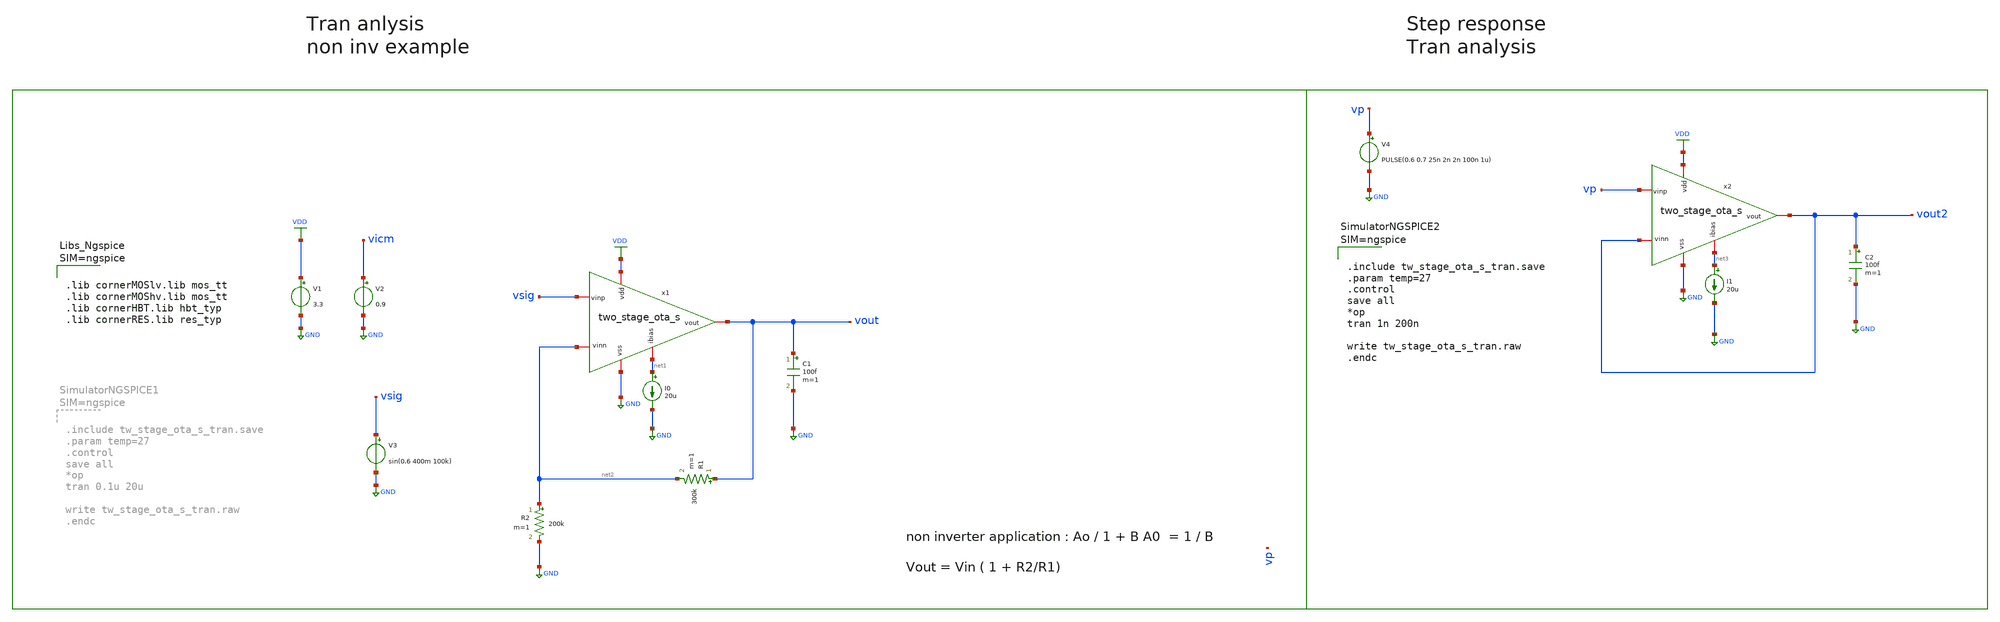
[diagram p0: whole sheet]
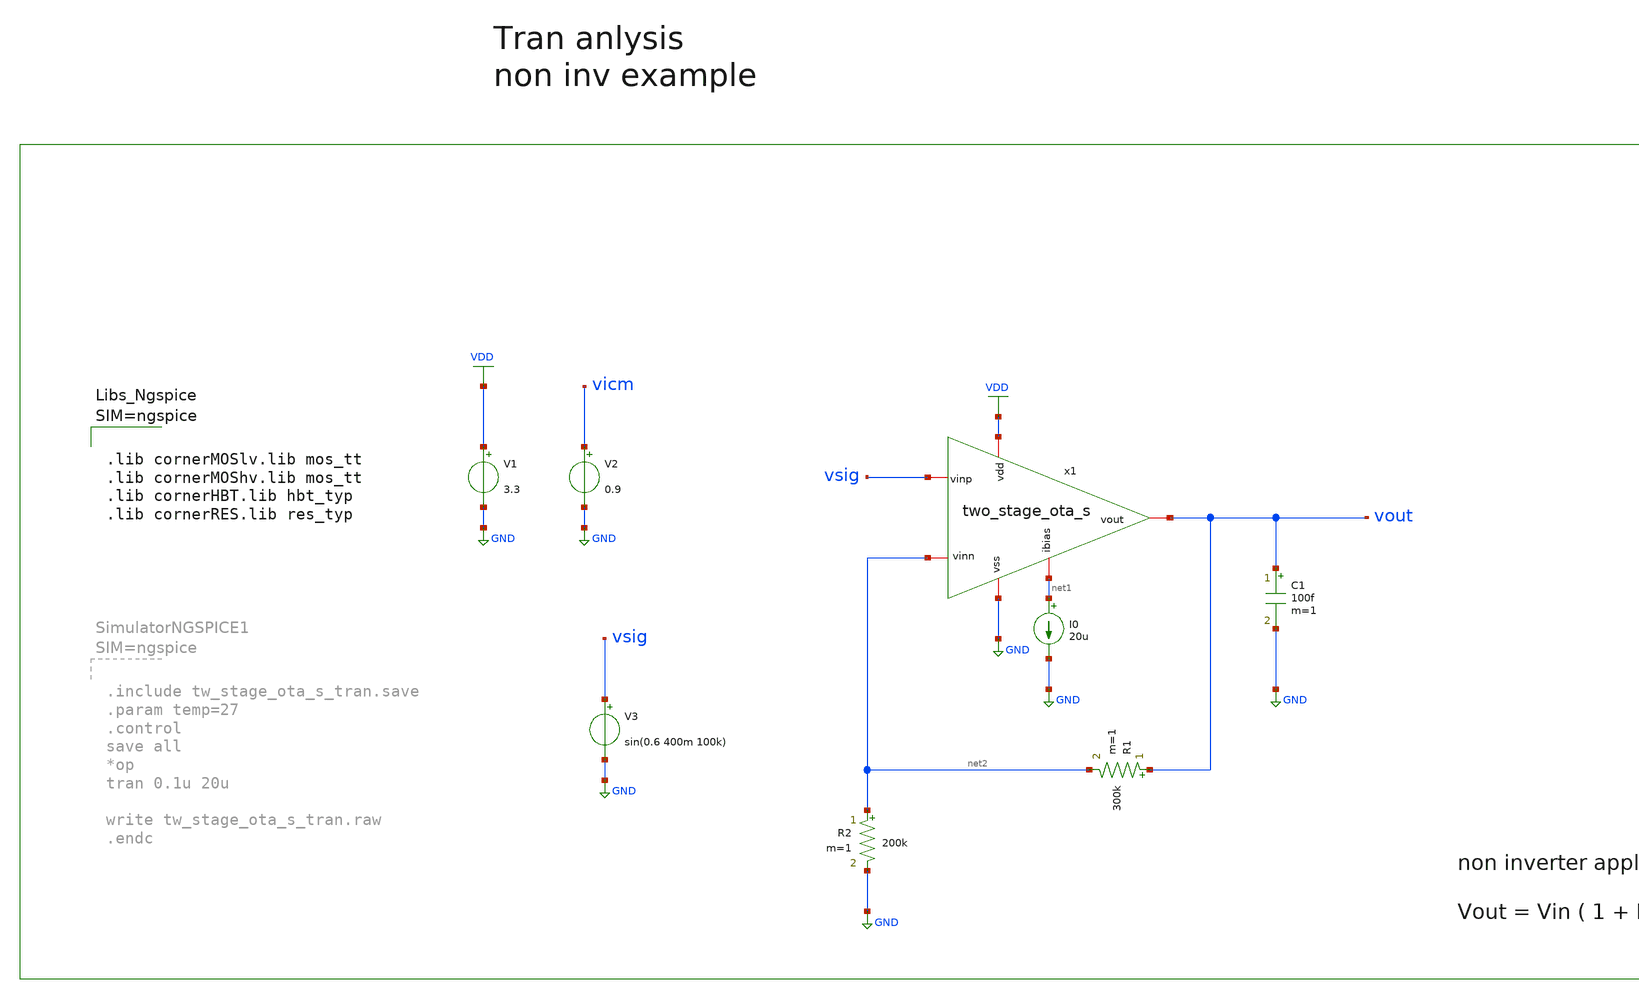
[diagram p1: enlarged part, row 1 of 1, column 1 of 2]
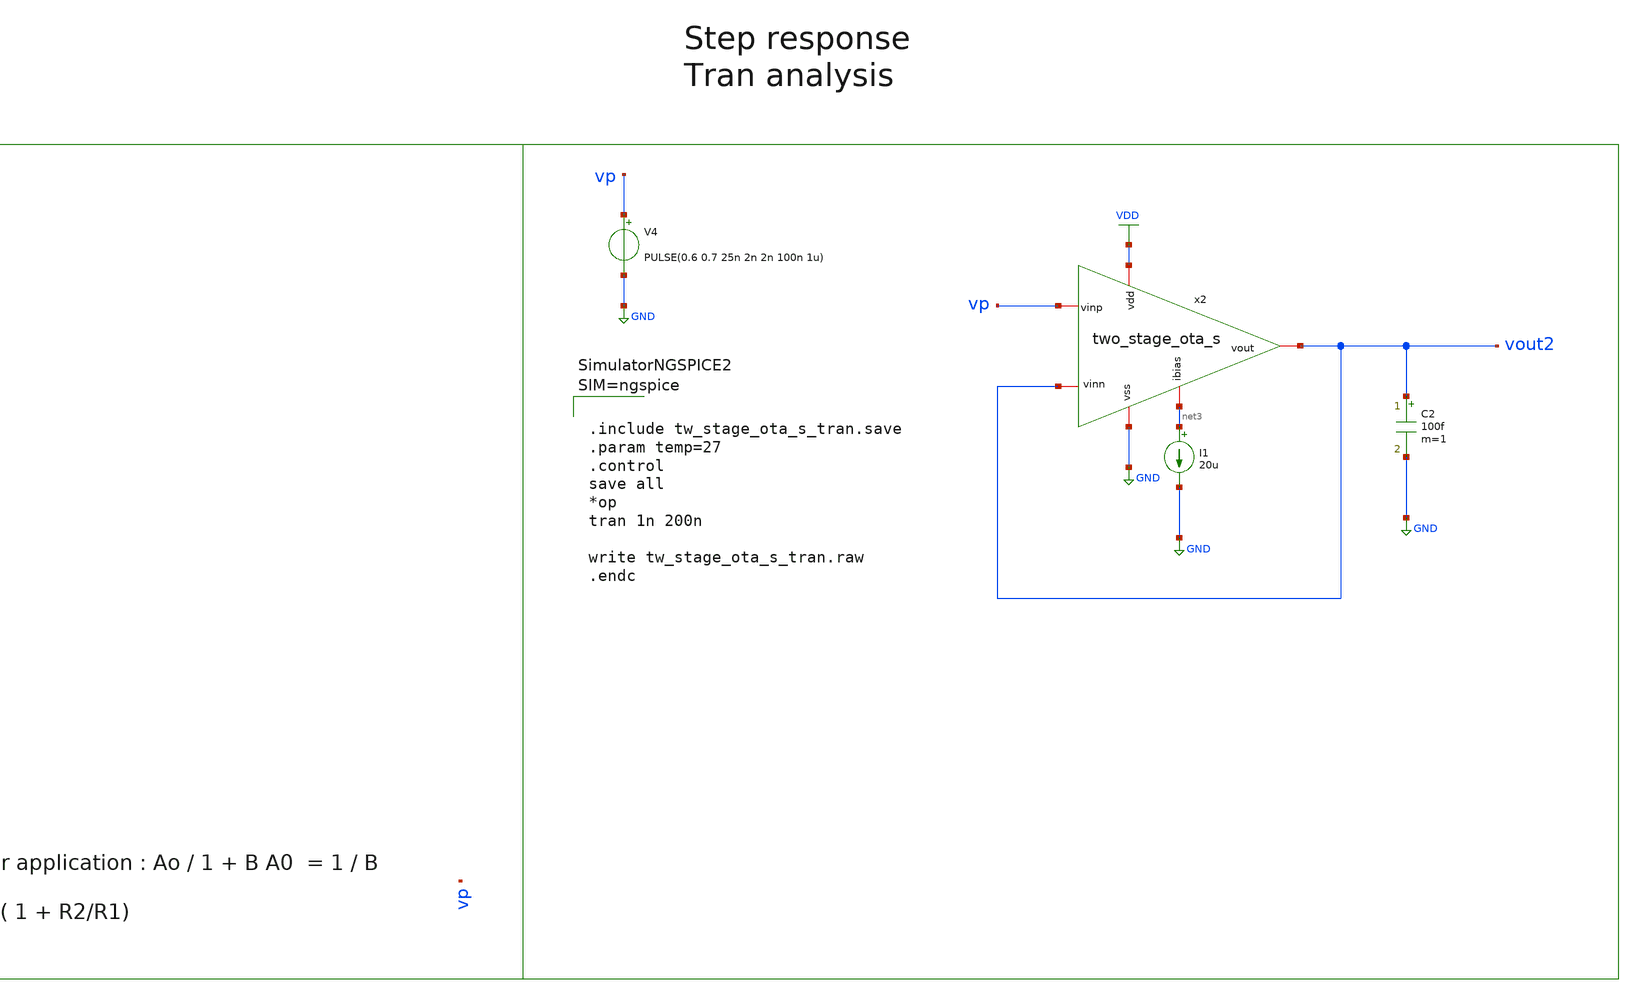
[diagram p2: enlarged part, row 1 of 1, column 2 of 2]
** sch_path: dependencies/pmu_ip/dependencies/OTA/OTA-main/testbenches/tw_stage_ota_s_tran.sch
* (c) 2025-2026 Ider Abdelaziz
**.subckt tw_stage_ota_s_tran
V1 VDD GND 3.3
V2 vicm GND 0.9
V3 vsig GND sin(0.6 400m 100k)
I0 net1 GND 20u
C1 vout GND 100f m=1
R1 vout net2 300k m=1
R2 net2 GND 200k m=1
x1 VDD net1 net2 vsig vout GND two_stage_ota_s
V4 vp GND PULSE(0.6 0.7 25n 2n 2n 100n 1u)
I1 net3 GND 20u
C2 vout2 GND 100f m=1
x2 VDD net3 vout2 vp vout2 GND two_stage_ota_s
**** begin user architecture code



.lib cornerMOSlv.lib mos_tt
.lib cornerMOShv.lib mos_tt
.lib cornerHBT.lib hbt_typ
.lib cornerRES.lib res_typ






.include tw_stage_ota_s_tran.save
.param temp=27
.control
save all
*op
tran 1n 200n

write tw_stage_ota_s_tran.raw
.endc



**** end user architecture code
**.ends

* expanding   symbol:  /foss/designs/bandgap_refrence_ihp/two_stage_ota/two_stage_ota_s.sym # of
*+ pins=6
** sym_path: dependencies/pmu_ip/dependencies/OTA/OTA-main/testbenches/two_stage_ota_s.sym
** sch_path: dependencies/pmu_ip/dependencies/OTA/OTA-main/testbenches/two_stage_ota_s.sch
.subckt two_stage_ota_s vdd ibias vinn vinp vout vss
*.iopin ibias
*.iopin vdd
*.iopin vss
*.iopin vout
*.iopin vinp
*.iopin vinn
C1 net4 vout 350f m=1
R1 net3 net4 4k m=1
XM4 net3 net2 vss vss sg13_hv_nmos w=3u l=1u ng=1 m=1 mm_ok=1
XM3 net2 net2 vss vss sg13_hv_nmos w=3u l=1u ng=1 m=1 mm_ok=1
XM1 net3 vinp net1 vdd sg13_hv_pmos w=12u l=1u ng=1 m=2 mm_ok=1
XM2 net2 vinn net1 vdd sg13_hv_pmos w=12u l=1u ng=1 m=2 mm_ok=1
XM5 net1 ibias vdd vdd sg13_hv_pmos w=6u l=3u ng=1 m=2 mm_ok=1
XM7 vout ibias vdd vdd sg13_hv_pmos w=6u l=3u ng=1 m=8 mm_ok=1
XM8 ibias ibias vdd vdd sg13_hv_pmos w=6u l=3u ng=1 m=8 mm_ok=1
XM9 vout net3 vss vss sg13_hv_nmos w=12u l=1u ng=1 m=2 mm_ok=1
.ends

.GLOBAL GND
.GLOBAL VDD
.end
